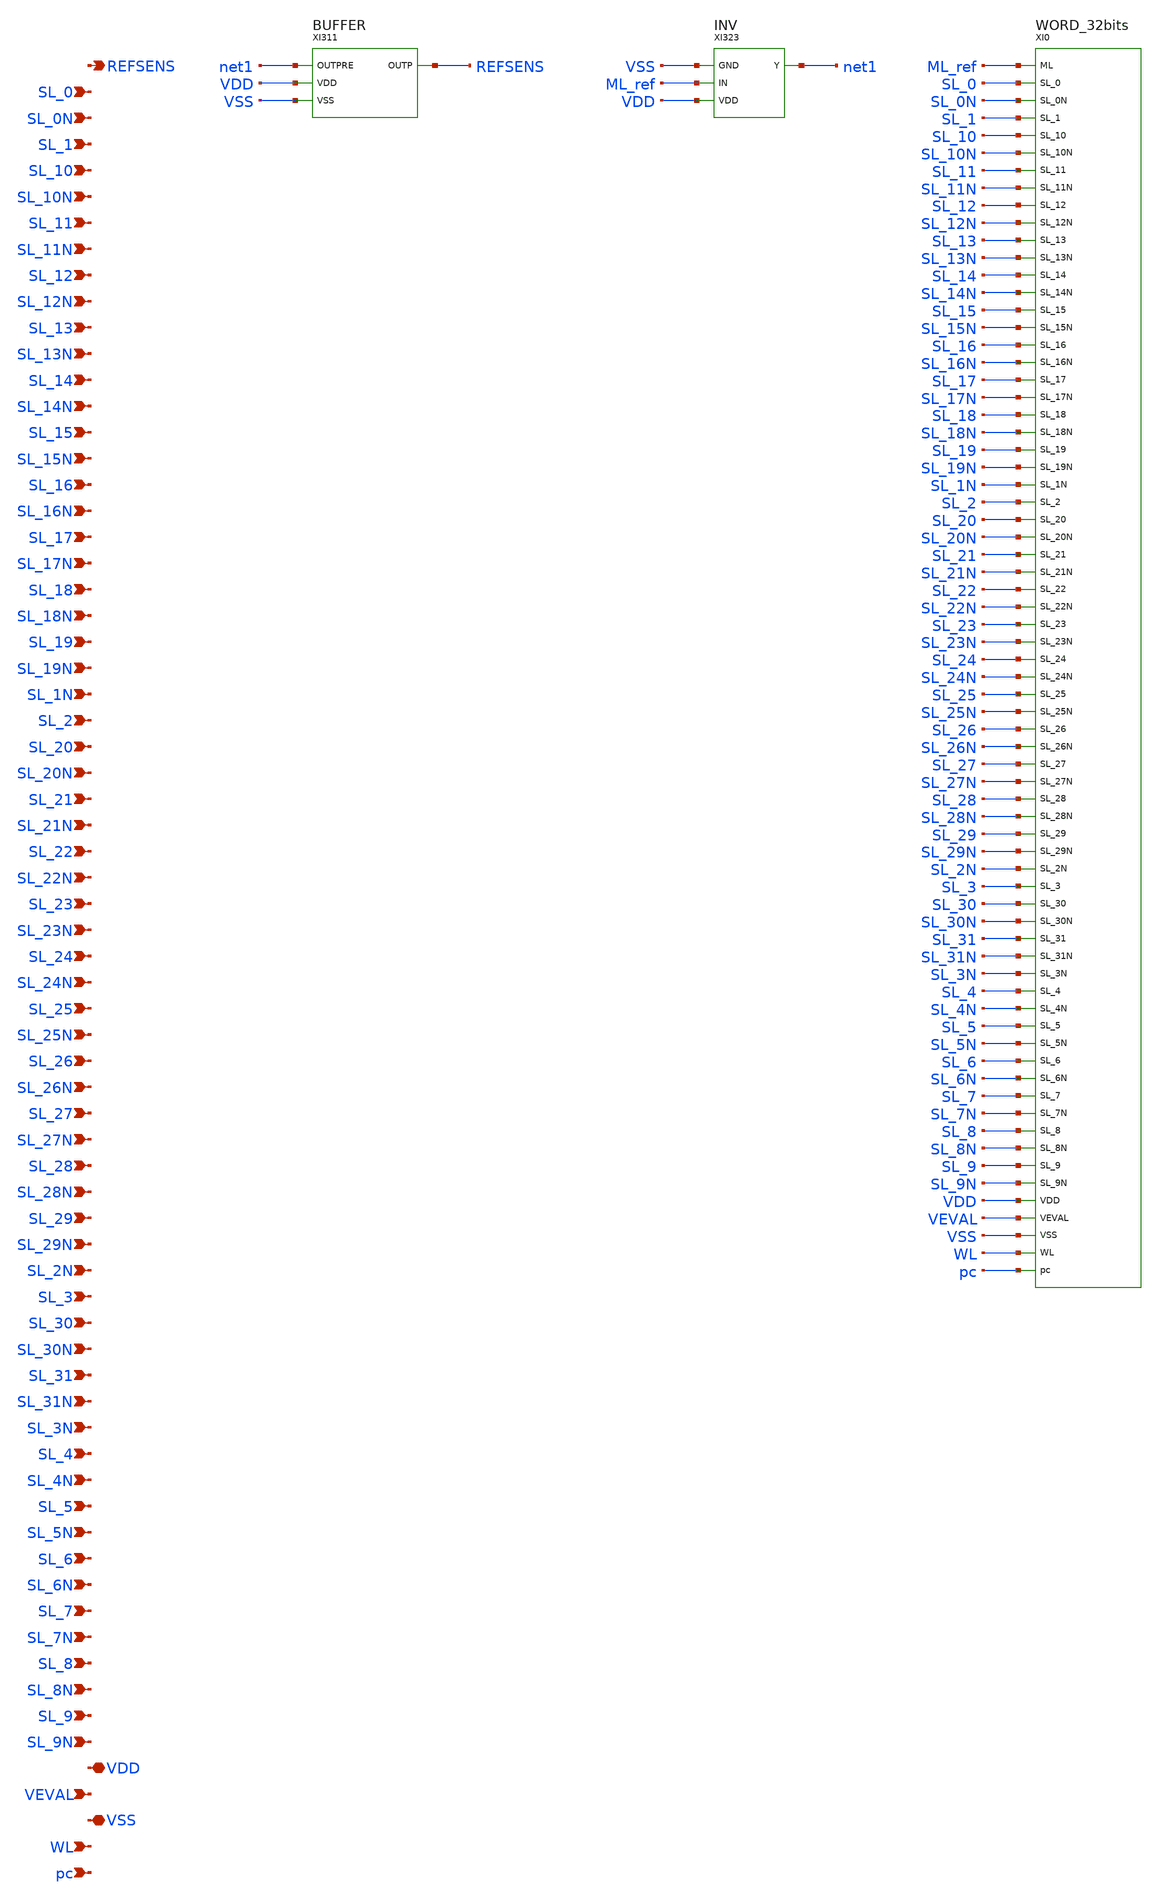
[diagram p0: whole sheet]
** sch_path: SoC6169-main/schematic/xschem/reference_complete.sch
* Copyright 2026 USFQ CAM team
* Licensed under the Apache License, Version 2.0 (the "License");
* you may not use this file except in compliance with the License.
* You may obtain a copy of the License at
* https://www.apache.org/licenses/LICENSE-2.0
* Unless required by applicable law or agreed to in writing, software
* distributed under the License is distributed on an "AS IS" BASIS,
* WITHOUT WARRANTIES OR CONDITIONS OF ANY KIND, either express or implied.
* See the License for the specific language governing permissions and
* limitations under the License.
**.subckt reference_complete REFSENS SL_0 SL_0N SL_1 SL_10 SL_10N SL_11 SL_11N SL_12 SL_12N SL_13
*+ SL_13N SL_14 SL_14N SL_15 SL_15N SL_16 SL_16N SL_17 SL_17N SL_18 SL_18N SL_19 SL_19N SL_1N SL_2 SL_20
*+ SL_20N SL_21 SL_21N SL_22 SL_22N SL_23 SL_23N SL_24 SL_24N SL_25 SL_25N SL_26 SL_26N SL_27 SL_27N SL_28
*+ SL_28N SL_29 SL_29N SL_2N SL_3 SL_30 SL_30N SL_31 SL_31N SL_3N SL_4 SL_4N SL_5 SL_5N SL_6 SL_6N SL_7 SL_7N
*+ SL_8 SL_8N SL_9 SL_9N VDD VEVAL VSS WL pc
*.opin REFSENS
*.ipin SL_0
*.ipin SL_0N
*.ipin SL_1
*.ipin SL_10
*.ipin SL_10N
*.ipin SL_11
*.ipin SL_11N
*.ipin SL_12
*.ipin SL_12N
*.ipin SL_13
*.ipin SL_13N
*.ipin SL_14
*.ipin SL_14N
*.ipin SL_15
*.ipin SL_15N
*.ipin SL_16
*.ipin SL_16N
*.ipin SL_17
*.ipin SL_17N
*.ipin SL_18
*.ipin SL_18N
*.ipin SL_19
*.ipin SL_19N
*.ipin SL_1N
*.ipin SL_2
*.ipin SL_20
*.ipin SL_20N
*.ipin SL_21
*.ipin SL_21N
*.ipin SL_22
*.ipin SL_22N
*.ipin SL_23
*.ipin SL_23N
*.ipin SL_24
*.ipin SL_24N
*.ipin SL_25
*.ipin SL_25N
*.ipin SL_26
*.ipin SL_26N
*.ipin SL_27
*.ipin SL_27N
*.ipin SL_28
*.ipin SL_28N
*.ipin SL_29
*.ipin SL_29N
*.ipin SL_2N
*.ipin SL_3
*.ipin SL_30
*.ipin SL_30N
*.ipin SL_31
*.ipin SL_31N
*.ipin SL_3N
*.ipin SL_4
*.ipin SL_4N
*.ipin SL_5
*.ipin SL_5N
*.ipin SL_6
*.ipin SL_6N
*.ipin SL_7
*.ipin SL_7N
*.ipin SL_8
*.ipin SL_8N
*.ipin SL_9
*.ipin SL_9N
*.iopin VDD
*.ipin VEVAL
*.iopin VSS
*.ipin WL
*.ipin pc
XI311 REFSENS net1 VDD VSS BUFFER
XI323 VSS ML_ref VDD net1 INV
XI0 ML_ref SL_0 SL_0N SL_1 SL_10 SL_10N SL_11 SL_11N SL_12 SL_12N SL_13 SL_13N SL_14 SL_14N SL_15
+ SL_15N SL_16 SL_16N SL_17 SL_17N SL_18 SL_18N SL_19 SL_19N SL_1N SL_2 SL_20 SL_20N SL_21 SL_21N SL_22
+ SL_22N SL_23 SL_23N SL_24 SL_24N SL_25 SL_25N SL_26 SL_26N SL_27 SL_27N SL_28 SL_28N SL_29 SL_29N SL_2N
+ SL_3 SL_30 SL_30N SL_31 SL_31N SL_3N SL_4 SL_4N SL_5 SL_5N SL_6 SL_6N SL_7 SL_7N SL_8 SL_8N SL_9 SL_9N
+ VDD VEVAL VSS WL pc WORD_32bits
**.ends

* expanding   symbol:  BUFFER.sym # of pins=4
** sym_path: SoC6169-main/schematic/xschem/BUFFER.sym
** sch_path: SoC6169-main/schematic/xschem/BUFFER.sch
.subckt BUFFER OUTP OUTPRE VDD VSS
*.opin OUTP
*.ipin OUTPRE
*.iopin VDD
*.iopin VSS
XMN0 OUTP medio VSS VSS sg13_lv_nmos w=3u l=130n ng=1 m=1 mm_ok=1
XMP0 OUTP medio VDD VDD sg13_lv_pmos w=6u l=130n ng=1 m=1 mm_ok=1
XI306 VSS OUTPRE VDD medio INV
.ends


* expanding   symbol:  INV.sym # of pins=4
** sym_path: SoC6169-main/schematic/xschem/INV.sym
** sch_path: SoC6169-main/schematic/xschem/INV.sch
.subckt INV GND IN VDD Y
*.iopin GND
*.ipin IN
*.iopin VDD
*.opin Y
XMN0 Y IN GND GND sg13_lv_nmos w=200n l=130n ng=1 m=1 mm_ok=1
XMP0 Y IN VDD VDD sg13_lv_pmos w=400n l=130n ng=1 m=1 mm_ok=1
.ends


* expanding   symbol:  WORD_32bits.sym # of pins=70
** sym_path: SoC6169-main/schematic/xschem/WORD_32bits.sym
** sch_path: SoC6169-main/schematic/xschem/WORD_32bits.sch
.subckt WORD_32bits ML SL_0 SL_0N SL_1 SL_10 SL_10N SL_11 SL_11N SL_12 SL_12N SL_13 SL_13N SL_14
+ SL_14N SL_15 SL_15N SL_16 SL_16N SL_17 SL_17N SL_18 SL_18N SL_19 SL_19N SL_1N SL_2 SL_20 SL_20N SL_21
+ SL_21N SL_22 SL_22N SL_23 SL_23N SL_24 SL_24N SL_25 SL_25N SL_26 SL_26N SL_27 SL_27N SL_28 SL_28N SL_29
+ SL_29N SL_2N SL_3 SL_30 SL_30N SL_31 SL_31N SL_3N SL_4 SL_4N SL_5 SL_5N SL_6 SL_6N SL_7 SL_7N SL_8 SL_8N
+ SL_9 SL_9N VDD VEVAL VSS WL pc
*.iopin ML
*.ipin SL_0
*.ipin SL_0N
*.ipin SL_1
*.ipin SL_10
*.ipin SL_10N
*.ipin SL_11
*.ipin SL_11N
*.ipin SL_12
*.ipin SL_12N
*.ipin SL_13
*.ipin SL_13N
*.ipin SL_14
*.ipin SL_14N
*.ipin SL_15
*.ipin SL_15N
*.ipin SL_16
*.ipin SL_16N
*.ipin SL_17
*.ipin SL_17N
*.ipin SL_18
*.ipin SL_18N
*.ipin SL_19
*.ipin SL_19N
*.ipin SL_1N
*.ipin SL_2
*.ipin SL_20
*.ipin SL_20N
*.ipin SL_21
*.ipin SL_21N
*.ipin SL_22
*.ipin SL_22N
*.ipin SL_23
*.ipin SL_23N
*.ipin SL_24
*.ipin SL_24N
*.ipin SL_25
*.ipin SL_25N
*.ipin SL_26
*.ipin SL_26N
*.ipin SL_27
*.ipin SL_27N
*.ipin SL_28
*.ipin SL_28N
*.ipin SL_29
*.ipin SL_29N
*.ipin SL_2N
*.ipin SL_3
*.ipin SL_30
*.ipin SL_30N
*.ipin SL_31
*.ipin SL_31N
*.ipin SL_3N
*.ipin SL_4
*.ipin SL_4N
*.ipin SL_5
*.ipin SL_5N
*.ipin SL_6
*.ipin SL_6N
*.ipin SL_7
*.ipin SL_7N
*.ipin SL_8
*.ipin SL_8N
*.ipin SL_9
*.ipin SL_9N
*.iopin VDD
*.ipin VEVAL
*.iopin VSS
*.ipin WL
*.ipin pc
XI31 ML SL_27 SL_27N VDD VEVAL VSS WL CELL
XI30 ML SL_24 SL_24N VDD VEVAL VSS WL CELL
XI29 ML SL_25 SL_25N VDD VEVAL VSS WL CELL
XI28 ML SL_26 SL_26N VDD VEVAL VSS WL CELL
XI27 ML SL_28 SL_28N VDD VEVAL VSS WL CELL
XI26 ML SL_29 SL_29N VDD VEVAL VSS WL CELL
XI25 ML SL_30 SL_30N VDD VEVAL VSS WL CELL
XI24 ML SL_31 SL_31N VDD VEVAL VSS WL CELL
XI23 ML SL_19 SL_19N VDD VEVAL VSS WL CELL
XI22 ML SL_16 SL_16N VDD VEVAL VSS WL CELL
XI21 ML SL_17 SL_17N VDD VEVAL VSS WL CELL
XI20 ML SL_18 SL_18N VDD VEVAL VSS WL CELL
XI19 ML SL_20 SL_20N VDD VEVAL VSS WL CELL
XI18 ML SL_21 SL_21N VDD VEVAL VSS WL CELL
XI17 ML SL_22 SL_22N VDD VEVAL VSS WL CELL
XI15 ML SL_11 SL_11N VDD VEVAL VSS WL CELL
XI14 ML SL_8 SL_8N VDD VEVAL VSS WL CELL
XI13 ML SL_9 SL_9N VDD VEVAL VSS WL CELL
XI12 ML SL_10 SL_10N VDD VEVAL VSS WL CELL
XI10 ML SL_12 SL_12N VDD VEVAL VSS WL CELL
XI6 ML SL_13 SL_13N VDD VEVAL VSS WL CELL
XI2 ML SL_14 SL_14N VDD VEVAL VSS WL CELL
XI1 ML SL_15 SL_15N VDD VEVAL VSS WL CELL
XI11 ML SL_3 SL_3N VDD VEVAL VSS WL CELL
XI9 ML SL_0 SL_0N VDD VEVAL VSS WL CELL
XI8 ML SL_1 SL_1N VDD VEVAL VSS WL CELL
XI7 ML SL_2 SL_2N VDD VEVAL VSS WL CELL
XI5 ML SL_4 SL_4N VDD VEVAL VSS WL CELL
XI4 ML SL_5 SL_5N VDD VEVAL VSS WL CELL
XI3 ML SL_6 SL_6N VDD VEVAL VSS WL CELL
XI0 ML SL_7 SL_7N VDD VEVAL VSS WL CELL
XI16 ML SL_23 SL_23N VDD VEVAL VSS WL CELL
XMP0 ML pc VDD VDD sg13_lv_pmos w=2u l=130n ng=1 m=1 mm_ok=1
.ends


* expanding   symbol:  CELL.sym # of pins=7
** sym_path: SoC6169-main/schematic/xschem/CELL.sym
** sch_path: SoC6169-main/schematic/xschem/CELL.sch
.subckt CELL ML SL SL_N VDD VEVAL VSS WL
*.iopin ML
*.ipin SL
*.ipin SL_N
*.iopin VDD
*.ipin VEVAL
*.iopin VSS
*.ipin WL
XI7 VSS net1 VDD net2 INV
XI4 VSS net2 VDD net1 INV
XMN5 net11 VEVAL VSS VSS sg13_lv_nmos w=350n l=130n ng=1 m=1 mm_ok=1
XMN4 net11 net3 ML VSS sg13_lv_nmos w=740n l=130n ng=1 m=1 mm_ok=1
XMN3 net3 net2 SL VSS sg13_lv_nmos w=740n l=130n ng=1 m=1 mm_ok=1
XMN2 net3 net1 SL_N VSS sg13_lv_nmos w=740n l=130n ng=1 m=1 mm_ok=1
XMN1 SL_N WL net1 VSS sg13_lv_nmos w=740n l=130n ng=1 m=1 mm_ok=1
XMN0 SL WL net2 VSS sg13_lv_nmos w=740n l=130n ng=1 m=1 mm_ok=1
.ends

.end
